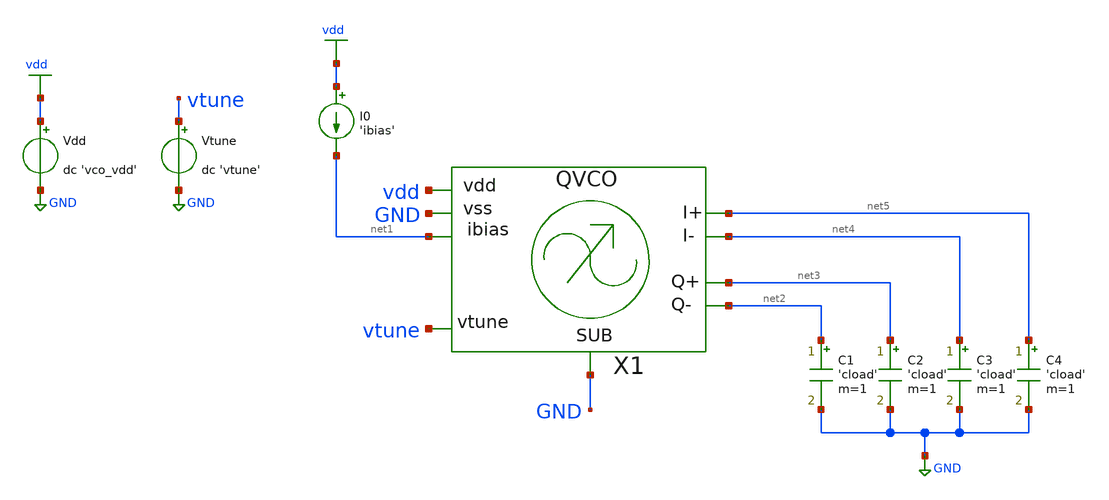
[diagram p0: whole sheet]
** sch_path: tb/vco/tb_startup.sch
**.subckt tb_startup
Vdd vdd GND dc 'vco_vdd'
Vtune vtune GND dc 'vtune'
X1 vdd GND vtune net5 net4 net3 net2 GND net1 vco m=1
I0 vdd net1 'ibias'
C1 net2 GND 'cload' m=1
C2 net3 GND 'cload' m=1
C3 net4 GND 'cload' m=1
C4 net5 GND 'cload' m=1
**** begin user architecture code


.include 'models_dir'/design.spice
.lib 'models_dir'/sm141064.spice 'mos_corner'
.lib 'models_dir'/sm141064.spice moscap_'mos_corner'
.option TEMP='temperature'
.option warn=1
.option rshunt=1e12
.option gmin=1e-6
Ikick net5 GND pulse(0 1u 0 20p 20p 20p 1)
.control
save all
tran 5p 8n
let i_diff = v(net5) - v(net4)
let q_diff = v(net3) - v(net2)
set wr_singlescale
wrdata 'simpath'/'filename'_'N'.data i_diff q_diff
quit
.endc


**** end user architecture code
**.ends
.GLOBAL GND
.GLOBAL vdd
.end
